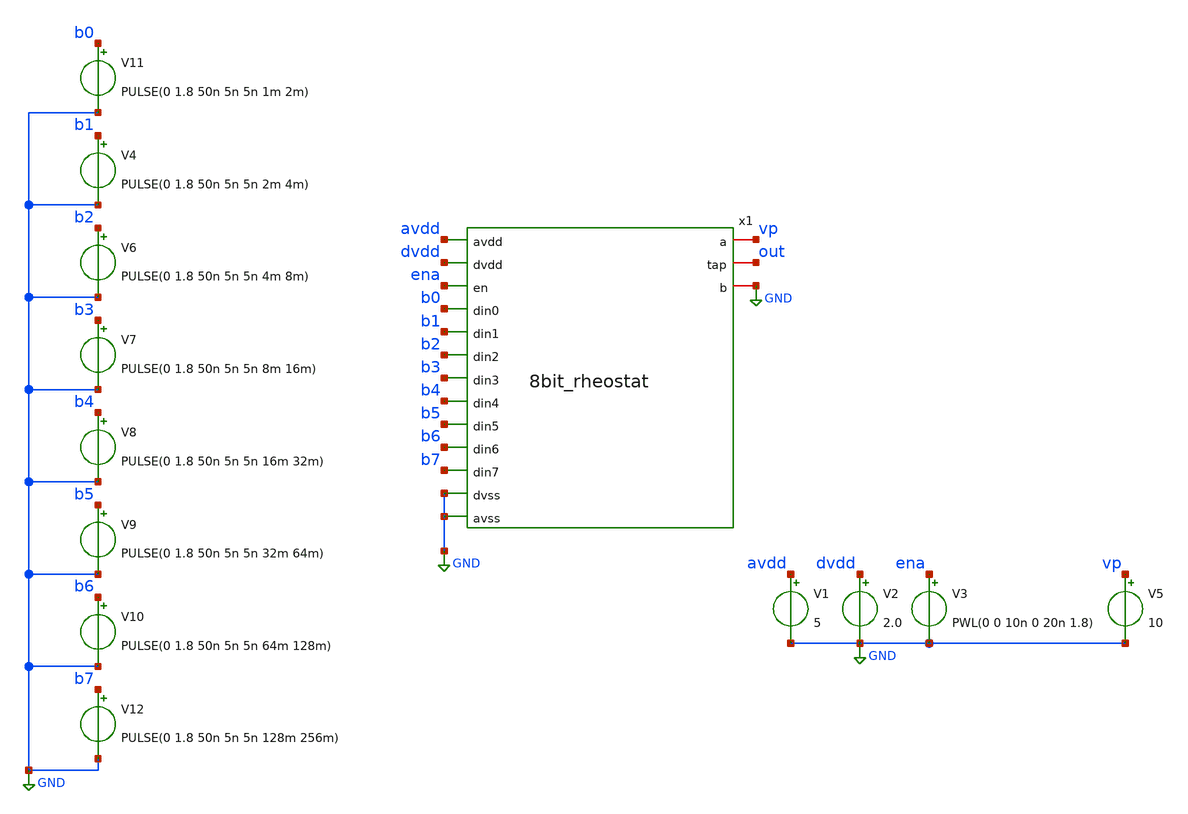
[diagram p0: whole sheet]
** sch_path: xschem/8bit_rheostat_tb.sch
**.subckt 8bit_rheostat_tb
x1 avdd dvdd vp ena b0 b1 out b2 b3 b4 GND b5 b6 b7 GND GND 8bit_rheostat
V11 b0 GND PULSE(0 1.8 50n 5n 5n 1m 2m)
V4 b1 GND PULSE(0 1.8 50n 5n 5n 2m 4m)
V6 b2 GND PULSE(0 1.8 50n 5n 5n 4m 8m)
V7 b3 GND PULSE(0 1.8 50n 5n 5n 8m 16m)
V8 b4 GND PULSE(0 1.8 50n 5n 5n 16m 32m)
V9 b5 GND PULSE(0 1.8 50n 5n 5n 32m 64m)
V10 b6 GND PULSE(0 1.8 50n 5n 5n 64m 128m)
V12 b7 GND PULSE(0 1.8 50n 5n 5n 128m 256m)
V1 avdd GND 5
V2 dvdd GND 2.0
V3 ena GND PWL(0 0 10n 0 20n 1.8)
V5 vp GND 10
**** begin user architecture code


.lib /usr/local/share/pdk/sky130A/libs.tech/ngspice/sky130.lib.spice tt
.include /usr/local/share/pdk/sky130A/libs.ref/sky130_fd_sc_hvl/spice/sky130_fd_sc_hvl.spice




.control
tran 1m 300m
plot V(out)
.endc

**** end user architecture code
**.ends

* expanding   symbol:  8bit_rheostat.sym # of pins=16
** sym_path: xschem/8bit_rheostat.sym
** sch_path: xschem/8bit_rheostat.sch
.subckt 8bit_rheostat avdd dvdd a en din0 din1 tap din2 din3 din4 b din5 din6 din7 dvss avss
*.ipin din0
*.ipin din1
*.ipin din2
*.ipin din3
*.ipin din4
*.ipin din5
*.ipin din6
*.ipin din7
*.iopin a
*.iopin tap
*.iopin b
*.ipin dvdd
*.ipin dvss
*.ipin avdd
*.ipin avss
*.ipin en
x1 avdd nb0 nb5 nb6 nb3 nb4 nb1 nb7 nb2 a tap pb3 pb2 pb4 pb1 pb5 pb7 pb6 pb0 avss
+ 8bit_half_rheostat
x2 dvdd nb0 en pb0 din0 dvss double_output_buffer
x3 dvdd nb1 en pb1 din1 dvss double_output_buffer
x4 dvdd nb2 en pb2 din2 dvss double_output_buffer
x5 dvdd nb3 en pb3 din3 dvss double_output_buffer
x6 dvdd nb4 en pb4 din4 dvss double_output_buffer
x7 dvdd nb5 en pb5 din5 dvss double_output_buffer
x8 dvdd nb6 en pb6 din6 dvss double_output_buffer
x9 dvdd nb7 en pb7 din7 dvss double_output_buffer
x10 avdd pb0 pb5 pb6 pb3 pb4 pb1 pb7 pb2 tap b nb3 nb2 nb4 nb1 nb5 nb7 nb6 nb0 avss
+ 8bit_half_rheostat
.ends


* expanding   symbol:  8bit_half_rheostat.sym # of pins=20
** sym_path: xschem/8bit_half_rheostat.sym
** sch_path: xschem/8bit_half_rheostat.sch
.subckt 8bit_half_rheostat avdd inn0 inn5 inn6 inn3 inn4 inn1 inn7 inn2 a b inp3 inp2 inp4 inp1 inp5
+ inp7 inp6 inp0 avss
*.iopin b
*.iopin a
*.ipin inn0
*.ipin inn1
*.ipin inn2
*.ipin inn3
*.ipin inn4
*.ipin inn5
*.ipin inn6
*.ipin inn7
*.ipin inp0
*.ipin inp1
*.ipin inp2
*.ipin inp3
*.ipin inp4
*.ipin inp5
*.ipin inp6
*.ipin inp7
*.ipin avdd
*.ipin avss
XM17 a inn0 net1 avdd sky130_fd_pr__pfet_g5v0d10v5 L=10 W=0.5 nf=1 ad='int((nf+1)/2) * W/nf * 0.29' as='int((nf+2)/2) * W/nf * 0.29'
+ pd='2*int((nf+1)/2) * (W/nf + 0.29)' ps='2*int((nf+2)/2) * (W/nf + 0.29)' nrd='0.29 / W' nrs='0.29 / W'
+ sa=0 sb=0 sd=0 mult=1 m=1
XM18 a inp0 net1 avss sky130_fd_pr__nfet_g5v0d10v5 L=0.5 W=10 nf=1 ad='int((nf+1)/2) * W/nf * 0.29' as='int((nf+2)/2) * W/nf * 0.29'
+ pd='2*int((nf+1)/2) * (W/nf + 0.29)' ps='2*int((nf+2)/2) * (W/nf + 0.29)' nrd='0.29 / W' nrs='0.29 / W'
+ sa=0 sb=0 sd=0 mult=1 m=1
XM19 net1 inn1 net2 avdd sky130_fd_pr__pfet_g5v0d10v5 L=10 W=0.5 nf=1 ad='int((nf+1)/2) * W/nf * 0.29'
+ as='int((nf+2)/2) * W/nf * 0.29' pd='2*int((nf+1)/2) * (W/nf + 0.29)' ps='2*int((nf+2)/2) * (W/nf + 0.29)'
+ nrd='0.29 / W' nrs='0.29 / W' sa=0 sb=0 sd=0 mult=1 m=1
XM20 net1 inp1 net2 avss sky130_fd_pr__nfet_g5v0d10v5 L=0.5 W=10 nf=1 ad='int((nf+1)/2) * W/nf * 0.29'
+ as='int((nf+2)/2) * W/nf * 0.29' pd='2*int((nf+1)/2) * (W/nf + 0.29)' ps='2*int((nf+2)/2) * (W/nf + 0.29)'
+ nrd='0.29 / W' nrs='0.29 / W' sa=0 sb=0 sd=0 mult=1 m=1
XM21 net2 inn2 net3 avdd sky130_fd_pr__pfet_g5v0d10v5 L=10 W=0.5 nf=1 ad='int((nf+1)/2) * W/nf * 0.29'
+ as='int((nf+2)/2) * W/nf * 0.29' pd='2*int((nf+1)/2) * (W/nf + 0.29)' ps='2*int((nf+2)/2) * (W/nf + 0.29)'
+ nrd='0.29 / W' nrs='0.29 / W' sa=0 sb=0 sd=0 mult=1 m=1
XM22 net2 inp2 net3 avss sky130_fd_pr__nfet_g5v0d10v5 L=0.5 W=10 nf=1 ad='int((nf+1)/2) * W/nf * 0.29'
+ as='int((nf+2)/2) * W/nf * 0.29' pd='2*int((nf+1)/2) * (W/nf + 0.29)' ps='2*int((nf+2)/2) * (W/nf + 0.29)'
+ nrd='0.29 / W' nrs='0.29 / W' sa=0 sb=0 sd=0 mult=1 m=1
XM23 net3 inn3 net4 avdd sky130_fd_pr__pfet_g5v0d10v5 L=10 W=0.5 nf=1 ad='int((nf+1)/2) * W/nf * 0.29'
+ as='int((nf+2)/2) * W/nf * 0.29' pd='2*int((nf+1)/2) * (W/nf + 0.29)' ps='2*int((nf+2)/2) * (W/nf + 0.29)'
+ nrd='0.29 / W' nrs='0.29 / W' sa=0 sb=0 sd=0 mult=1 m=1
XM24 net3 inp3 net4 avss sky130_fd_pr__nfet_g5v0d10v5 L=0.5 W=10 nf=1 ad='int((nf+1)/2) * W/nf * 0.29'
+ as='int((nf+2)/2) * W/nf * 0.29' pd='2*int((nf+1)/2) * (W/nf + 0.29)' ps='2*int((nf+2)/2) * (W/nf + 0.29)'
+ nrd='0.29 / W' nrs='0.29 / W' sa=0 sb=0 sd=0 mult=1 m=1
XM25 net4 inn4 net5 avdd sky130_fd_pr__pfet_g5v0d10v5 L=10 W=0.5 nf=1 ad='int((nf+1)/2) * W/nf * 0.29'
+ as='int((nf+2)/2) * W/nf * 0.29' pd='2*int((nf+1)/2) * (W/nf + 0.29)' ps='2*int((nf+2)/2) * (W/nf + 0.29)'
+ nrd='0.29 / W' nrs='0.29 / W' sa=0 sb=0 sd=0 mult=1 m=1
XM26 net4 inp4 net5 avss sky130_fd_pr__nfet_g5v0d10v5 L=0.5 W=10 nf=1 ad='int((nf+1)/2) * W/nf * 0.29'
+ as='int((nf+2)/2) * W/nf * 0.29' pd='2*int((nf+1)/2) * (W/nf + 0.29)' ps='2*int((nf+2)/2) * (W/nf + 0.29)'
+ nrd='0.29 / W' nrs='0.29 / W' sa=0 sb=0 sd=0 mult=1 m=1
XM27 net5 inn5 net6 avdd sky130_fd_pr__pfet_g5v0d10v5 L=10 W=0.5 nf=1 ad='int((nf+1)/2) * W/nf * 0.29'
+ as='int((nf+2)/2) * W/nf * 0.29' pd='2*int((nf+1)/2) * (W/nf + 0.29)' ps='2*int((nf+2)/2) * (W/nf + 0.29)'
+ nrd='0.29 / W' nrs='0.29 / W' sa=0 sb=0 sd=0 mult=1 m=1
XM28 net5 inp5 net6 avss sky130_fd_pr__nfet_g5v0d10v5 L=0.5 W=10 nf=1 ad='int((nf+1)/2) * W/nf * 0.29'
+ as='int((nf+2)/2) * W/nf * 0.29' pd='2*int((nf+1)/2) * (W/nf + 0.29)' ps='2*int((nf+2)/2) * (W/nf + 0.29)'
+ nrd='0.29 / W' nrs='0.29 / W' sa=0 sb=0 sd=0 mult=1 m=1
XM29 net6 inn6 net7 avdd sky130_fd_pr__pfet_g5v0d10v5 L=10 W=0.5 nf=1 ad='int((nf+1)/2) * W/nf * 0.29'
+ as='int((nf+2)/2) * W/nf * 0.29' pd='2*int((nf+1)/2) * (W/nf + 0.29)' ps='2*int((nf+2)/2) * (W/nf + 0.29)'
+ nrd='0.29 / W' nrs='0.29 / W' sa=0 sb=0 sd=0 mult=1 m=1
XM30 net6 inp6 net7 avss sky130_fd_pr__nfet_g5v0d10v5 L=0.5 W=10 nf=1 ad='int((nf+1)/2) * W/nf * 0.29'
+ as='int((nf+2)/2) * W/nf * 0.29' pd='2*int((nf+1)/2) * (W/nf + 0.29)' ps='2*int((nf+2)/2) * (W/nf + 0.29)'
+ nrd='0.29 / W' nrs='0.29 / W' sa=0 sb=0 sd=0 mult=1 m=1
XM31 net7 inn7 b avdd sky130_fd_pr__pfet_g5v0d10v5 L=10 W=0.5 nf=1 ad='int((nf+1)/2) * W/nf * 0.29' as='int((nf+2)/2) * W/nf * 0.29'
+ pd='2*int((nf+1)/2) * (W/nf + 0.29)' ps='2*int((nf+2)/2) * (W/nf + 0.29)' nrd='0.29 / W' nrs='0.29 / W'
+ sa=0 sb=0 sd=0 mult=1 m=1
XM32 net7 inp7 b avss sky130_fd_pr__nfet_g5v0d10v5 L=0.5 W=10 nf=1 ad='int((nf+1)/2) * W/nf * 0.29' as='int((nf+2)/2) * W/nf * 0.29'
+ pd='2*int((nf+1)/2) * (W/nf + 0.29)' ps='2*int((nf+2)/2) * (W/nf + 0.29)' nrd='0.29 / W' nrs='0.29 / W'
+ sa=0 sb=0 sd=0 mult=1 m=1
XR9 a net1 sky130_fd_pr__res_generic_po W=0.957 L=2 m=1
XR10 net1 net2 sky130_fd_pr__res_generic_po W=0.957 L=4 m=1
XR11 net2 net3 sky130_fd_pr__res_generic_po W=0.957 L=8 m=1
XR12 net3 net4 sky130_fd_pr__res_generic_po W=0.957 L=16 m=1
XR13 net4 net5 sky130_fd_pr__res_generic_po W=0.957 L=32 m=1
XR14 net5 net6 sky130_fd_pr__res_generic_po W=0.957 L=64 m=1
XR15 net6 net7 sky130_fd_pr__res_generic_po W=0.957 L=128 m=1
XR16 net7 b sky130_fd_pr__res_generic_po W=0.957 L=256 m=1
.ends


* expanding   symbol:  double_output_buffer.sym # of pins=6
** sym_path: xschem/double_output_buffer.sym
** sch_path: xschem/double_output_buffer.sch
.subckt double_output_buffer dvdd nout en pout din dvss
*.ipin din
*.ipin dvdd
*.ipin dvss
*.opin pout
*.opin nout
*.ipin en
XM1 nout en dvdd dvdd sky130_fd_pr__pfet_01v8 L=0.15 W=1 nf=1 ad='int((nf+1)/2) * W/nf * 0.29' as='int((nf+2)/2) * W/nf * 0.29'
+ pd='2*int((nf+1)/2) * (W/nf + 0.29)' ps='2*int((nf+2)/2) * (W/nf + 0.29)' nrd='0.29 / W' nrs='0.29 / W'
+ sa=0 sb=0 sd=0 mult=1 m=1
XM2 nout din dvdd dvdd sky130_fd_pr__pfet_01v8 L=0.15 W=1 nf=1 ad='int((nf+1)/2) * W/nf * 0.29' as='int((nf+2)/2) * W/nf * 0.29'
+ pd='2*int((nf+1)/2) * (W/nf + 0.29)' ps='2*int((nf+2)/2) * (W/nf + 0.29)' nrd='0.29 / W' nrs='0.29 / W'
+ sa=0 sb=0 sd=0 mult=1 m=1
XM3 pout nout dvdd dvdd sky130_fd_pr__pfet_01v8 L=0.15 W=1 nf=1 ad='int((nf+1)/2) * W/nf * 0.29' as='int((nf+2)/2) * W/nf * 0.29'
+ pd='2*int((nf+1)/2) * (W/nf + 0.29)' ps='2*int((nf+2)/2) * (W/nf + 0.29)' nrd='0.29 / W' nrs='0.29 / W'
+ sa=0 sb=0 sd=0 mult=1 m=1
XM4 nout en net1 dvss sky130_fd_pr__nfet_01v8 L=0.15 W=1 nf=1 ad='int((nf+1)/2) * W/nf * 0.29' as='int((nf+2)/2) * W/nf * 0.29'
+ pd='2*int((nf+1)/2) * (W/nf + 0.29)' ps='2*int((nf+2)/2) * (W/nf + 0.29)' nrd='0.29 / W' nrs='0.29 / W'
+ sa=0 sb=0 sd=0 mult=1 m=1
XM5 net1 din dvss dvss sky130_fd_pr__nfet_01v8 L=0.15 W=1 nf=1 ad='int((nf+1)/2) * W/nf * 0.29' as='int((nf+2)/2) * W/nf * 0.29'
+ pd='2*int((nf+1)/2) * (W/nf + 0.29)' ps='2*int((nf+2)/2) * (W/nf + 0.29)' nrd='0.29 / W' nrs='0.29 / W'
+ sa=0 sb=0 sd=0 mult=1 m=1
XM6 pout nout dvss dvss sky130_fd_pr__nfet_01v8 L=0.15 W=1 nf=1 ad='int((nf+1)/2) * W/nf * 0.29' as='int((nf+2)/2) * W/nf * 0.29'
+ pd='2*int((nf+1)/2) * (W/nf + 0.29)' ps='2*int((nf+2)/2) * (W/nf + 0.29)' nrd='0.29 / W' nrs='0.29 / W'
+ sa=0 sb=0 sd=0 mult=1 m=1
.ends

.GLOBAL GND
.end
